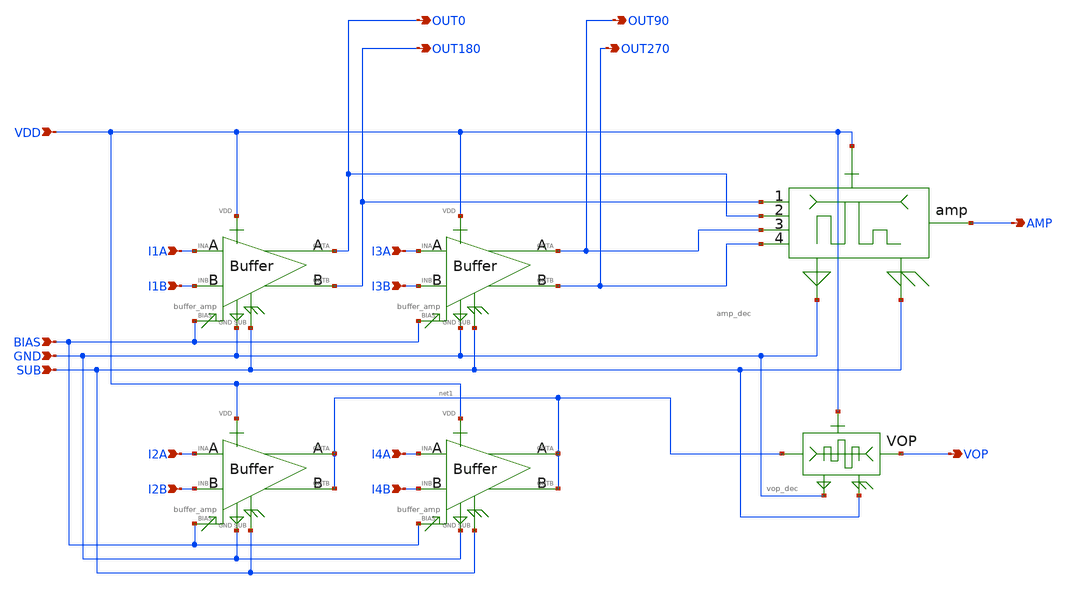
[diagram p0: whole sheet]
** sch_path: xschem/buffer_amp_vop.sch
**.subckt buffer_amp_vop BIAS GND SUB I1A I1B I2A I2B I3A I3B I4A I4B VDD AMP VOP OUT0 OUT180 OUT90
*+ OUT270
*.ipin BIAS
*.ipin GND
*.ipin SUB
*.ipin I1A
*.ipin I1B
*.ipin I2A
*.ipin I2B
*.ipin I3A
*.ipin I3B
*.ipin I4A
*.ipin I4B
*.ipin VDD
*.opin AMP
*.opin VOP
*.opin OUT0
*.opin OUT180
*.opin OUT90
*.opin OUT270
X2 I2A I2B BIAS VDD GND SUB net1 net1 buffer_amp
X4 I4A I4B BIAS VDD GND SUB net1 net1 buffer_amp
X1 I1A I1B BIAS VDD GND SUB OUT0 OUT180 buffer_amp
X3 I3A I3B BIAS VDD GND SUB OUT90 OUT270 buffer_amp
X5 OUT180 OUT0 OUT90 OUT270 AMP VDD GND SUB amp_dec
X6 net1 VDD GND SUB VOP vop_dec
**.ends

* expanding   symbol:  buffer_amp.sym # of pins=8
** sym_path: buffer_amp.sym
** sch_path: buffer_amp.sch
.subckt buffer_amp INA INB BIAS VDD GND SUB OUTA OUTB
*.ipin INA
*.ipin INB
*.ipin BIAS
*.ipin GND
*.ipin VDD
*.ipin SUB
*.opin OUTA
*.opin OUTB
XM1 net1 BIAS GND SUB sky130_fd_pr__nfet_01v8_lvt L=0.15 W=10 nf=10 ad='int((nf+1)/2) * W/nf * 0.29'
+ as='int((nf+2)/2) * W/nf * 0.29' pd='2*int((nf+1)/2) * (W/nf + 0.29)' ps='2*int((nf+2)/2) * (W/nf + 0.29)'
+ nrd='0.29 / W' nrs='0.29 / W' sa=0 sb=0 sd=0 mult=1 m=1
XM2 OUTB INB net1 SUB sky130_fd_pr__nfet_01v8_lvt L=0.15 W=1 nf=1 ad='int((nf+1)/2) * W/nf * 0.29' as='int((nf+2)/2) * W/nf * 0.29'
+ pd='2*int((nf+1)/2) * (W/nf + 0.29)' ps='2*int((nf+2)/2) * (W/nf + 0.29)' nrd='0.29 / W' nrs='0.29 / W'
+ sa=0 sb=0 sd=0 mult=1 m=1
XM3 OUTA INA net1 SUB sky130_fd_pr__nfet_01v8_lvt L=0.15 W=1 nf=1 ad='int((nf+1)/2) * W/nf * 0.29' as='int((nf+2)/2) * W/nf * 0.29'
+ pd='2*int((nf+1)/2) * (W/nf + 0.29)' ps='2*int((nf+2)/2) * (W/nf + 0.29)' nrd='0.29 / W' nrs='0.29 / W'
+ sa=0 sb=0 sd=0 mult=1 m=1
XR2 OUTB VDD SUB sky130_fd_pr__res_high_po_5p73 L=30.4 mult=1 m=1
XR1 OUTA VDD SUB sky130_fd_pr__res_high_po_5p73 L=30.4 mult=1 m=1
XM4 net1 BIAS GND SUB sky130_fd_pr__nfet_01v8_lvt L=0.15 W=10 nf=10 ad='int((nf+1)/2) * W/nf * 0.29'
+ as='int((nf+2)/2) * W/nf * 0.29' pd='2*int((nf+1)/2) * (W/nf + 0.29)' ps='2*int((nf+2)/2) * (W/nf + 0.29)'
+ nrd='0.29 / W' nrs='0.29 / W' sa=0 sb=0 sd=0 mult=1 m=1
.ends


* expanding   symbol:  amp_dec.sym # of pins=8
** sym_path: amp_dec.sym
** sch_path: amp_dec.sch
.subckt amp_dec IN1 IN2 IN3 IN4 AMP VDD GND SUB
*.ipin VDD
*.ipin SUB
*.ipin GND
*.ipin IN1
*.ipin IN2
*.ipin IN3
*.ipin IN4
*.opin AMP
XM25 VDD IN1 AMP SUB sky130_fd_pr__nfet_01v8_lvt L=0.15 W=4 nf=4 ad='int((nf+1)/2) * W/nf * 0.29' as='int((nf+2)/2) * W/nf * 0.29'
+ pd='2*int((nf+1)/2) * (W/nf + 0.29)' ps='2*int((nf+2)/2) * (W/nf + 0.29)' nrd='0.29 / W' nrs='0.29 / W'
+ sa=0 sb=0 sd=0 mult=1 m=1
XC1 AMP GND sky130_fd_pr__cap_mim_m3_1 W=20 L=30 MF=1 m=1
XM26 VDD IN2 AMP SUB sky130_fd_pr__nfet_01v8_lvt L=0.15 W=4 nf=4 ad='int((nf+1)/2) * W/nf * 0.29' as='int((nf+2)/2) * W/nf * 0.29'
+ pd='2*int((nf+1)/2) * (W/nf + 0.29)' ps='2*int((nf+2)/2) * (W/nf + 0.29)' nrd='0.29 / W' nrs='0.29 / W'
+ sa=0 sb=0 sd=0 mult=1 m=1
XM27 VDD IN3 AMP SUB sky130_fd_pr__nfet_01v8_lvt L=0.15 W=4 nf=4 ad='int((nf+1)/2) * W/nf * 0.29' as='int((nf+2)/2) * W/nf * 0.29'
+ pd='2*int((nf+1)/2) * (W/nf + 0.29)' ps='2*int((nf+2)/2) * (W/nf + 0.29)' nrd='0.29 / W' nrs='0.29 / W'
+ sa=0 sb=0 sd=0 mult=1 m=1
XM28 VDD IN4 AMP SUB sky130_fd_pr__nfet_01v8_lvt L=0.15 W=4 nf=4 ad='int((nf+1)/2) * W/nf * 0.29' as='int((nf+2)/2) * W/nf * 0.29'
+ pd='2*int((nf+1)/2) * (W/nf + 0.29)' ps='2*int((nf+2)/2) * (W/nf + 0.29)' nrd='0.29 / W' nrs='0.29 / W'
+ sa=0 sb=0 sd=0 mult=1 m=1
XR18 GND AMP SUB sky130_fd_pr__res_high_po_2p85 L=42 mult=1 m=1
.ends


* expanding   symbol:  vop_dec.sym # of pins=5
** sym_path: vop_dec.sym
** sch_path: vop_dec.sch
.subckt vop_dec IN VDD GND SUB VOP
*.ipin IN
*.ipin VDD
*.ipin GND
*.ipin SUB
*.opin VOP
XM41 VDD IN VOP SUB sky130_fd_pr__nfet_01v8_lvt L=0.15 W=12 nf=12 ad='int((nf+1)/2) * W/nf * 0.29' as='int((nf+2)/2) * W/nf * 0.29'
+ pd='2*int((nf+1)/2) * (W/nf + 0.29)' ps='2*int((nf+2)/2) * (W/nf + 0.29)' nrd='0.29 / W' nrs='0.29 / W'
+ sa=0 sb=0 sd=0 mult=1 m=1
XC2 IN GND sky130_fd_pr__cap_mim_m3_1 W=20 L=30 MF=1 m=1
XR21 GND VOP SUB sky130_fd_pr__res_high_po_2p85 L=42 mult=1 m=1
.ends

.end
